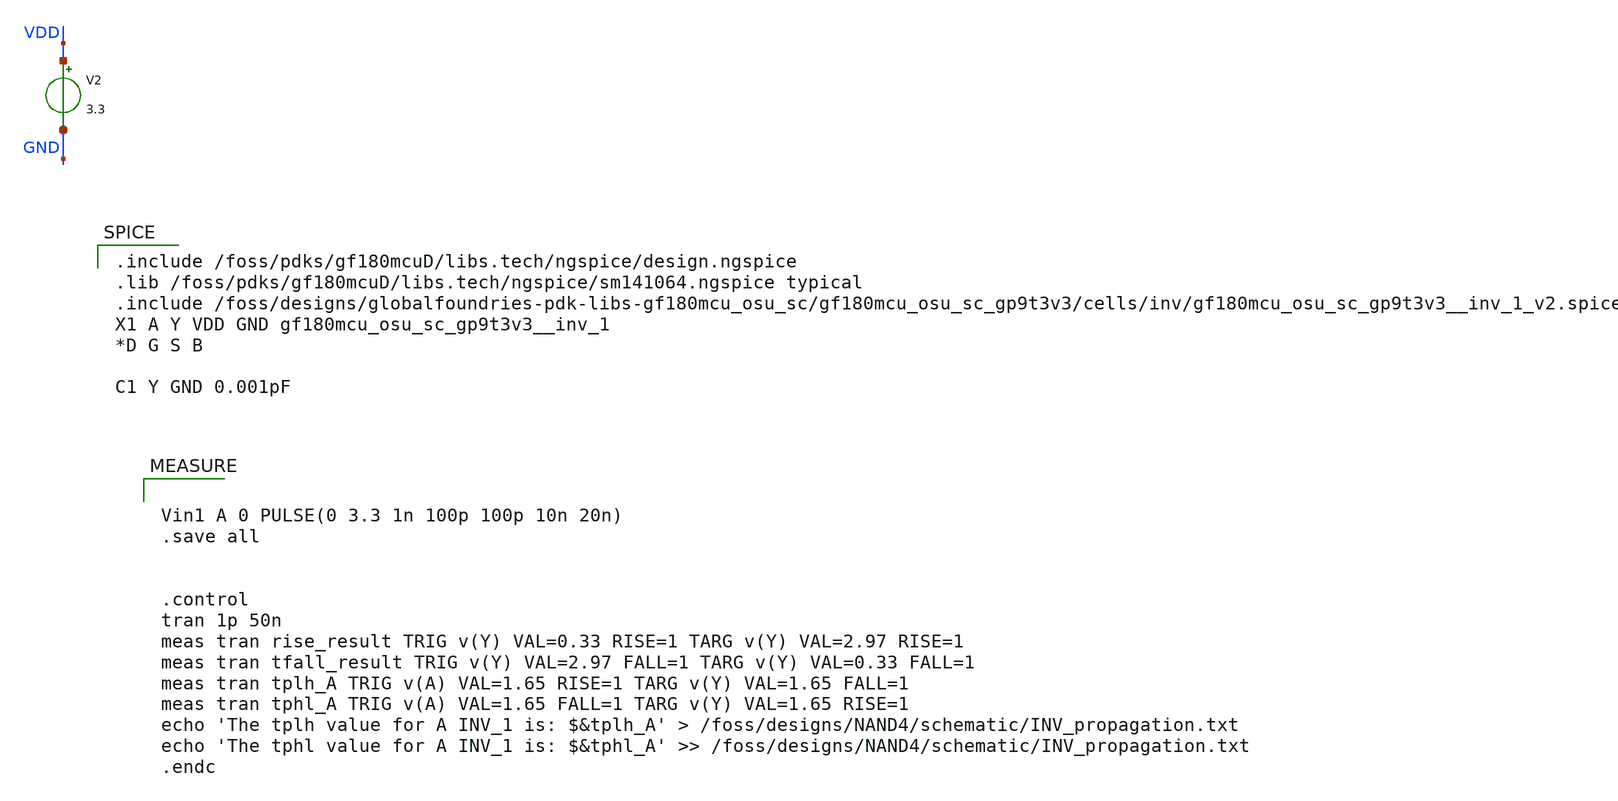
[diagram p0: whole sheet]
** sch_path: designs/libs/tb_archive/existingSC_Test/inverter.sch
**.subckt inverter
V2 VDD GND 3.3
**** begin user architecture code

.include /foss/pdks/gf180mcuD/libs.tech/ngspice/design.ngspice
.lib /foss/pdks/gf180mcuD/libs.tech/ngspice/sm141064.ngspice typical
.include /foss/designs/globalfoundries-pdk-libs-gf180mcu_osu_sc/gf180mcu_osu_sc_gp9t3v3/cells/inv/gf180mcu_osu_sc_gp9t3v3__inv_1_v2.spice
X1 A Y VDD GND gf180mcu_osu_sc_gp9t3v3__inv_1
*D G S B

C1 Y GND 0.001pF






Vin1 A 0 PULSE(0 3.3 1n 100p 100p 10n 20n)
.save all


.control
tran 1p 50n
meas tran rise_result TRIG v(Y) VAL=0.33 RISE=1 TARG v(Y) VAL=2.97 RISE=1
meas tran tfall_result TRIG v(Y) VAL=2.97 FALL=1 TARG v(Y) VAL=0.33 FALL=1
meas tran tplh_A TRIG v(A) VAL=1.65 RISE=1 TARG v(Y) VAL=1.65 FALL=1
meas tran tphl_A TRIG v(A) VAL=1.65 FALL=1 TARG v(Y) VAL=1.65 RISE=1
echo 'The tplh value for A INV_1 is: $&tplh_A' > /foss/designs/NAND4/schematic/INV_propagation.txt
echo 'The tphl value for A INV_1 is: $&tphl_A' >> /foss/designs/NAND4/schematic/INV_propagation.txt
.endc



**** end user architecture code
**.ends
.end
